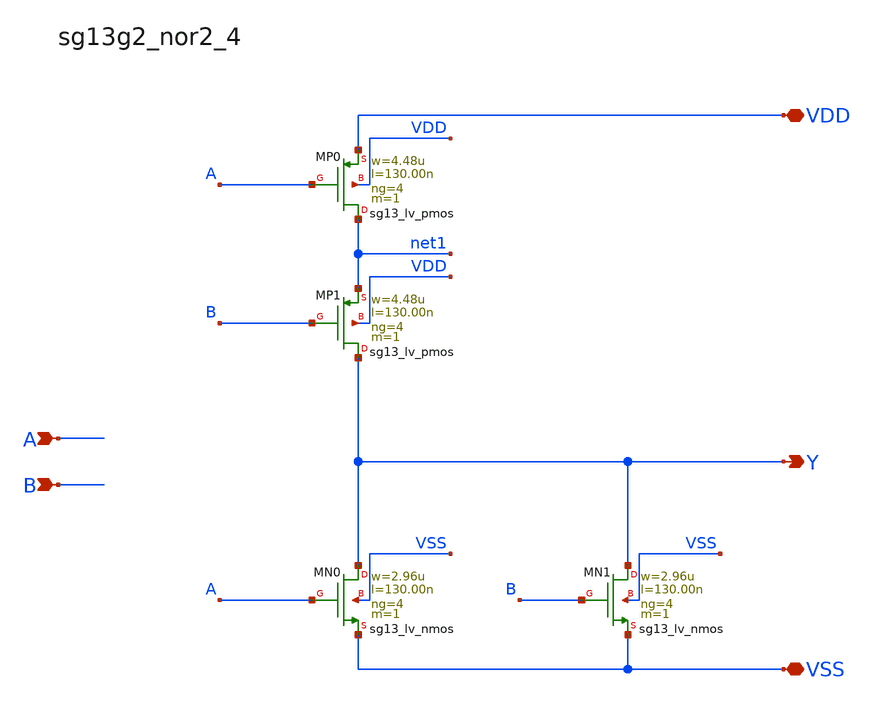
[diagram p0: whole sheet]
** sch_path: outputs/sg13g2_cells/cells/sg13g2_nor2_4/sg13g2_nor2_4.sch
**.subckt sg13g2_nor2_4 Y A B VDD VSS
*.opin Y
*.ipin A
*.ipin B
*.iopin VDD
*.iopin VSS
XMN0 Y A VSS VSS sg13_lv_nmos w=2.96u l=130.00n ng=4 m=1 mm_ok=1
XMN1 Y B VSS VSS sg13_lv_nmos w=2.96u l=130.00n ng=4 m=1 mm_ok=1
XMP0 net1 A VDD VDD sg13_lv_pmos w=4.48u l=130.00n ng=4 m=1 mm_ok=1
XMP1 Y B net1 VDD sg13_lv_pmos w=4.48u l=130.00n ng=4 m=1 mm_ok=1
**.ends
.end
